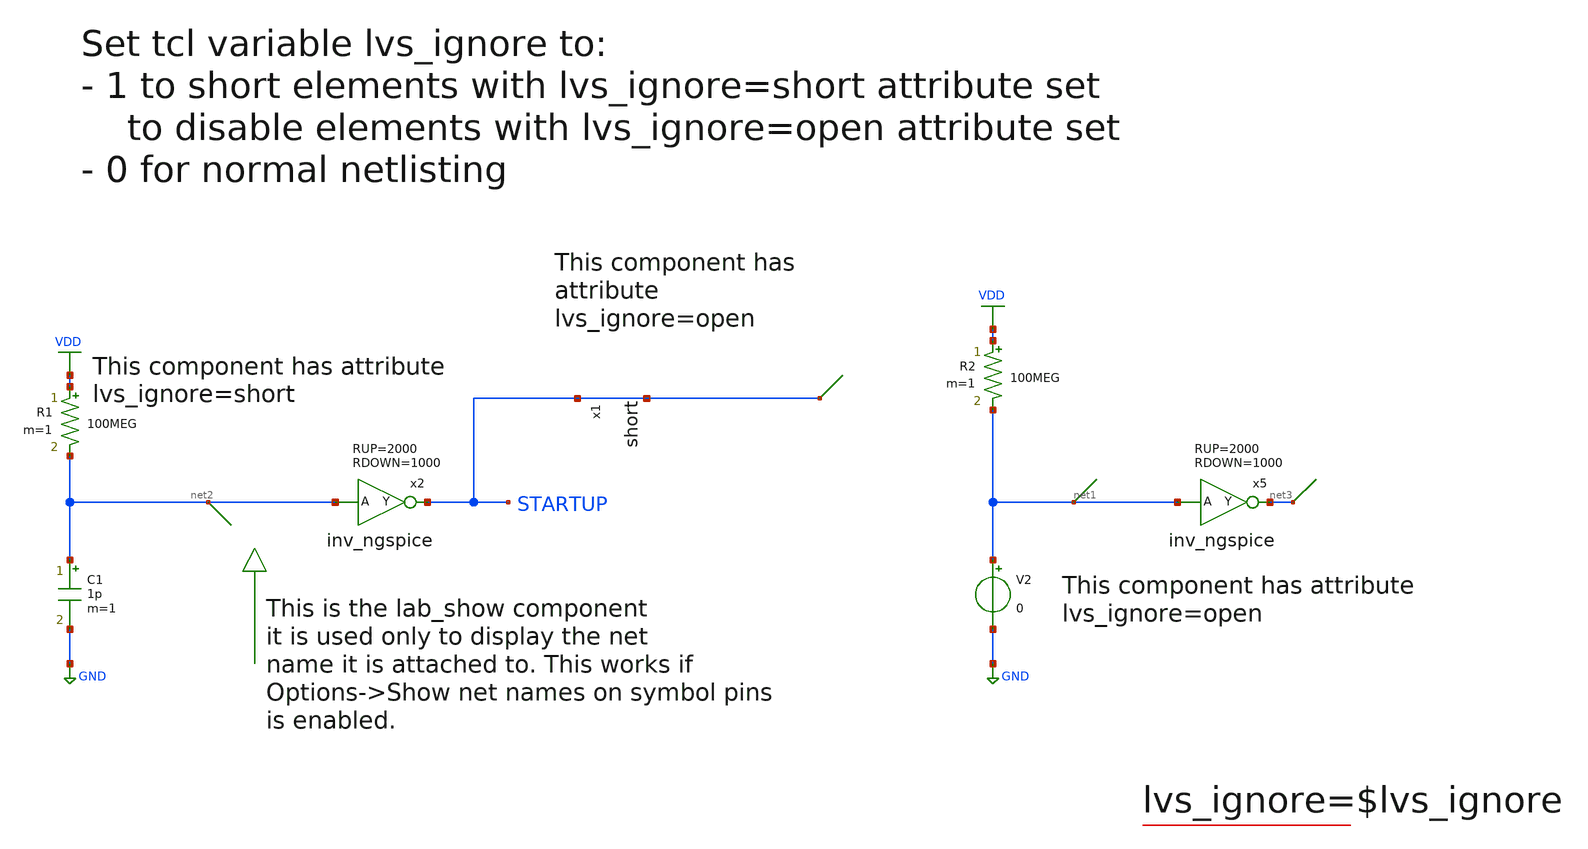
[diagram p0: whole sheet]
** sch_path: xschem-src/xschem_library/examples/test_lvs_ignore.sch
* Copyright (C) 1998-2026 Stefan Frederik Schippers
* This program is free software; you can redistribute it and/or modify
* it under the terms of the GNU General Public License as published by
* the Free Software Foundation; either version 2 of the License, or
* (at your option) any later version.
* This program is distributed in the hope that it will be useful,
* but WITHOUT ANY WARRANTY; without even the implied warranty of
* MERCHANTABILITY or FITNESS FOR A PARTICULAR PURPOSE.  See the
* GNU General Public License for more details.
* You should have received a copy of the GNU General Public License
* along with this program; if not, write to the Free Software
**.subckt test_lvs_ignore
V2 net1 GND 0
x5 net3 net1 inv_ngspice RUP=2000 RDOWN=1000
R1 VDD net2 100MEG m=1
C1 net2 GND 1p m=1
x2 STARTUP net2 inv_ngspice RUP=2000 RDOWN=1000
R2 VDD net1 100MEG m=1
* short x1 : STARTUP <--> STARTUP
**.ends

* expanding   symbol:  inv_ngspice.sym # of pins=2
** sym_path: xschem-src/xschem_library/ngspice/inv_ngspice.sym
** sch_path: xschem-src/xschem_library/ngspice/inv_ngspice.sch
.subckt inv_ngspice Y A  RUP=2000 RDOWN=1000
*.ipin A
*.opin Y
B1 X1 0 V = 'VCC/2*(1-tanh((V(A1)-VCC/2)*100))'
C1 A1 0 8f m=1
C2 Y1 0 8f m=1
V1 Y Y1 0
.save i(v1)
V2 A1 A 0
.save i(v2)
B2 X1 Y1 I = 'v(X1,Y1) > 0 ? v(X1,Y1) / RUP : v(X1,Y1) / RDOWN'
.ends

.GLOBAL GND
.GLOBAL VDD
.end
